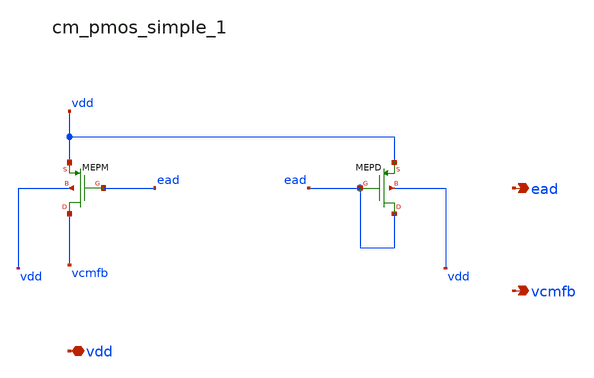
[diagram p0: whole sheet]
** sch_path: analog-db/raw/amp_023_fer_fd2s/hier/blocks/cm_pmos_simple_1.sch
**.subckt cm_pmos_simple_1 vdd ead vcmfb
*.iopin vdd
*.opin ead
*.opin vcmfb
XMEPD ead ead vdd vdd sg13_lv_pmos w=x_dut_xmepd_w l=x_dut_xmepd_l ng=1 m=x_dut_xmepd_m
XMEPM vcmfb ead vdd vdd sg13_lv_pmos w=x_dut_xmepm_w l=x_dut_xmepm_l ng=1 m=x_dut_xmepm_m
**.ends
.end
